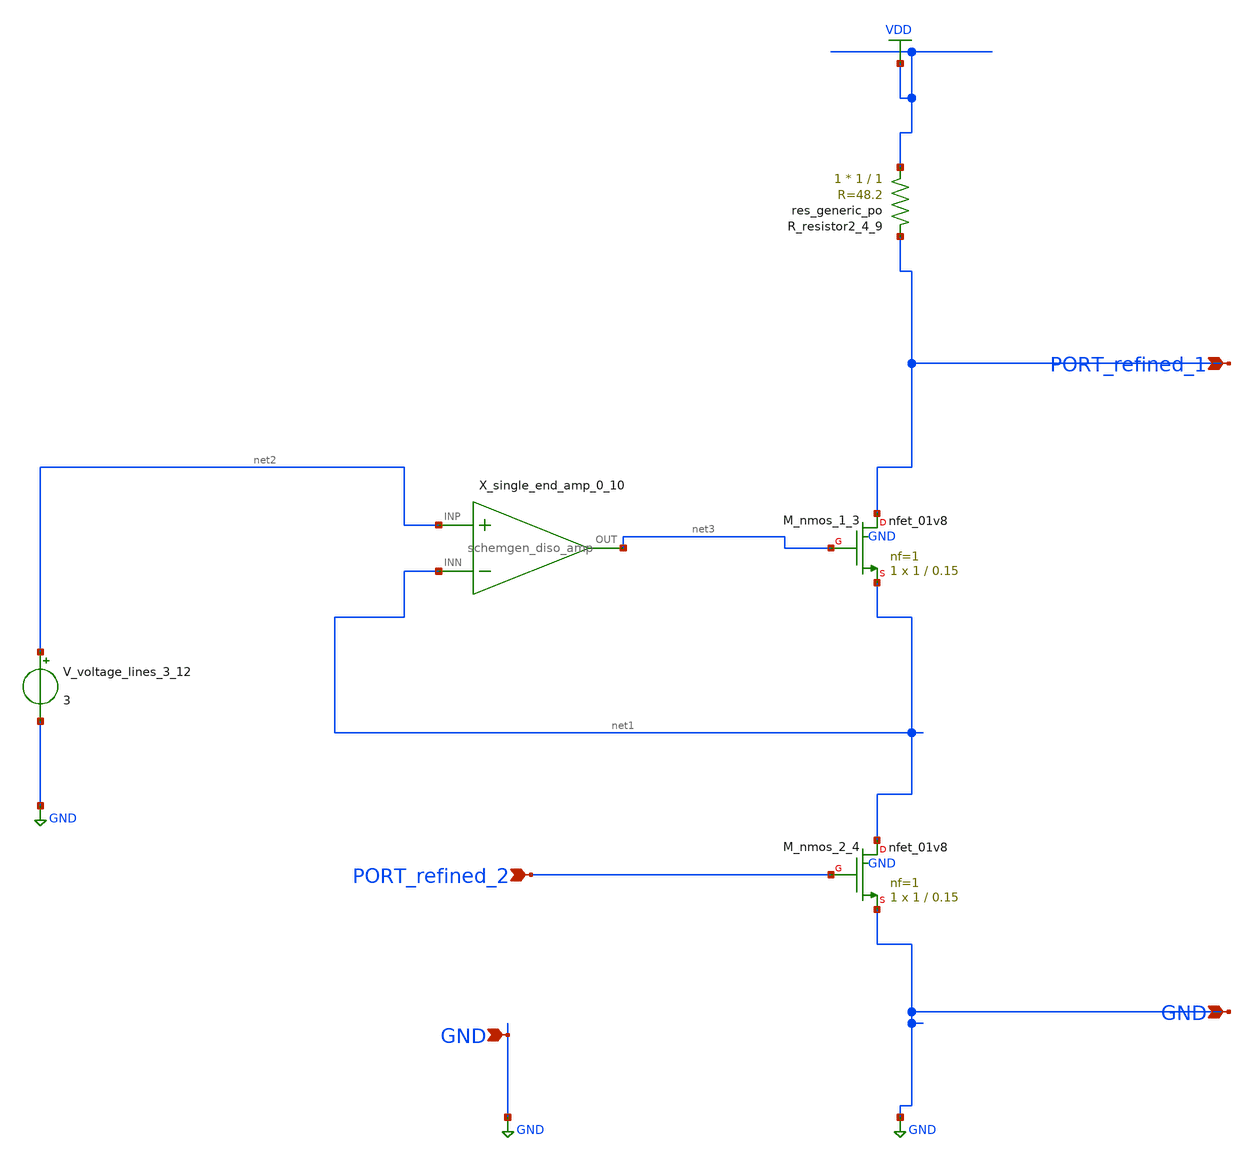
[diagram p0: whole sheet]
** sch_path: schematics/Image2Net/002.sch
**.subckt 002 GND PORT_refined_1 PORT_refined_2 GND
*.ipin GND
*.ipin PORT_refined_1
*.ipin PORT_refined_2
*.ipin GND
XM_nmos_1_3 PORT_refined_1 net3 net1 GND sky130_fd_pr__nfet_01v8 L=0.15 W=1 nf=1 ad='int((1 + 1)/2) * 1 / 1 * 0.29'
+ as='int((1 + 2)/2) * 1 / 1 * 0.29' pd='2*int((1 + 1)/2) * (1 / 1 + 0.29)' ps='2*int((1 + 2)/2) * (1 / 1 + 0.29)'
+ nrd='0.29 / 1 ' nrs='0.29 / 1 ' sa=0 sb=0 sd=0 mult=1 m=1
XM_nmos_2_4 net1 PORT_refined_2 GND GND sky130_fd_pr__nfet_01v8 L=0.15 W=1 nf=1 ad='int((1 + 1)/2) * 1 / 1 * 0.29'
+ as='int((1 + 2)/2) * 1 / 1 * 0.29' pd='2*int((1 + 1)/2) * (1 / 1 + 0.29)' ps='2*int((1 + 2)/2) * (1 / 1 + 0.29)'
+ nrd='0.29 / 1 ' nrs='0.29 / 1 ' sa=0 sb=0 sd=0 mult=1 m=1
XR_resistor2_4_9 VDD PORT_refined_1 sky130_fd_pr__res_generic_po W=1 L=1 m=1
X_single_end_amp_0_10 net2 net1 net3 schemgen_diso_amp
V_voltage_lines_3_12 net2 GND 3
**.ends

* expanding   symbol:  schemgen_diso_amp.sym # of pins=3
** sym_path: symbols/schemgen_diso_amp.sym
.subckt schemgen_diso_amp INP INN OUT
* SchemGen ideal op-amp: Vout = 1e5 * (V(INP) - V(INN))
E1 OUT 0 INP INN 1e5
.ends schemgen_diso_amp
.GLOBAL GND
.GLOBAL VDD
.end
